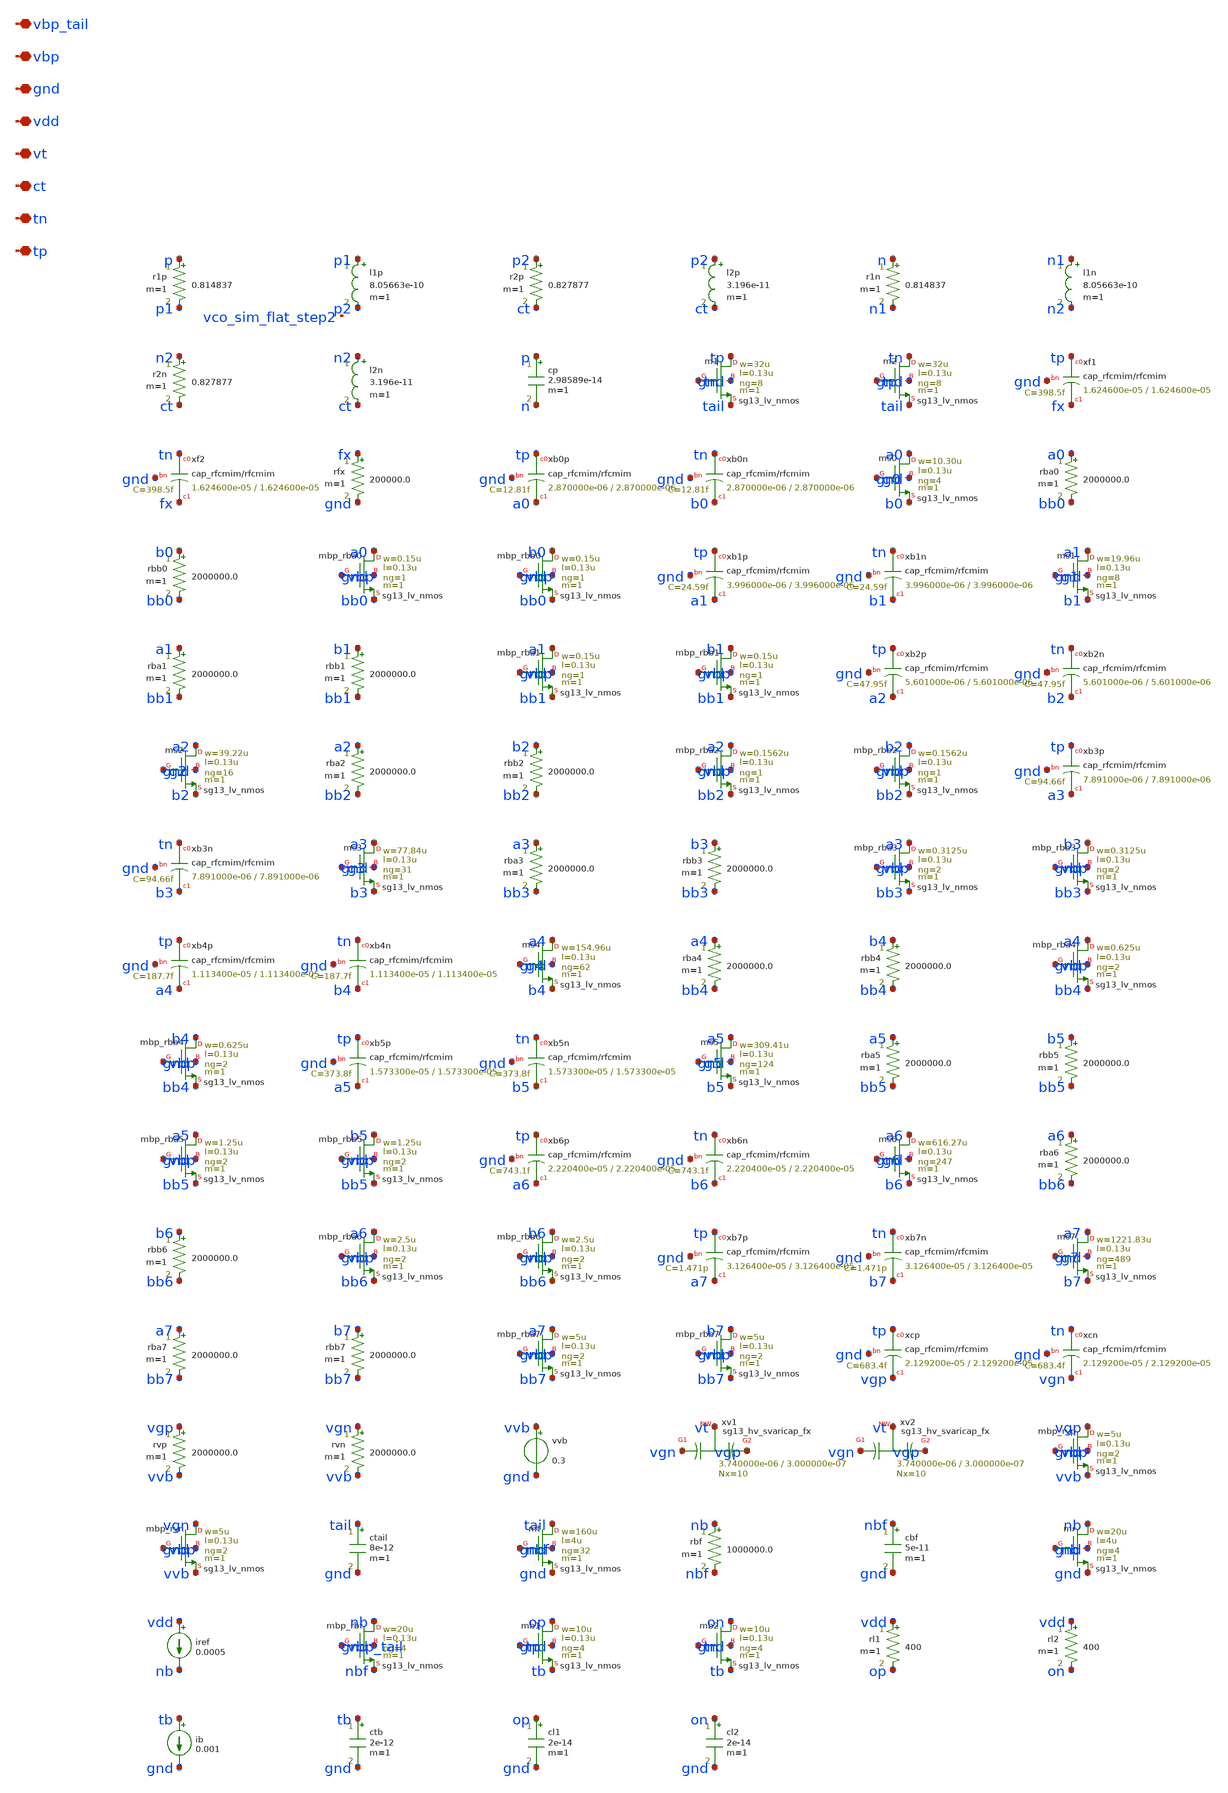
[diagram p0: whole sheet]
** sch_path: analog/vco/sch/vco_sim_flat.sch
**.subckt vco_sim_flat tp tn ct vt vdd gnd vbp vbp_tail
*.iopin tp
*.iopin tn
*.iopin ct
*.iopin vt
*.iopin vdd
*.iopin gnd
*.iopin vbp
*.iopin vbp_tail
r1p p p1 0.814837 m=1
l1p p1 p2 8.05663e-10 m=1
r2p p2 ct 0.827877 m=1
l2p p2 ct 3.196e-11 m=1
r1n n n1 0.814837 m=1
l1n n1 n2 8.05663e-10 m=1
r2n n2 ct 0.827877 m=1
l2n n2 ct 3.196e-11 m=1
cp p n 2.98589e-14 m=1
Xm1 tp tn tail gnd sg13_lv_nmos w=32u l=0.13u ng=8 m=1 mm_ok=1
Xm2 tn tp tail gnd sg13_lv_nmos w=32u l=0.13u ng=8 m=1 mm_ok=1
Xxf1 tp fx gnd cap_rfcmim w=1.624600e-05 l=1.624600e-05 wfeed=5.0e-6 m=1 mm_ok=1
Xxf2 tn fx gnd cap_rfcmim w=1.624600e-05 l=1.624600e-05 wfeed=5.0e-6 m=1 mm_ok=1
rfx fx gnd 200000.0 m=1
Xxb0p tp a0 gnd cap_rfcmim w=2.870000e-06 l=2.870000e-06 wfeed=5.0e-6 m=1 mm_ok=1
Xxb0n tn b0 gnd cap_rfcmim w=2.870000e-06 l=2.870000e-06 wfeed=5.0e-6 m=1 mm_ok=1
Xms0 a0 g0 b0 gnd sg13_lv_nmos w=10.30u l=0.13u ng=4 m=1 mm_ok=1
rba0 a0 bb0 2000000.0 m=1
rbb0 b0 bb0 2000000.0 m=1
Xmbp_rba0 a0 vbp bb0 gnd sg13_lv_nmos w=0.15u l=0.13u ng=1 m=1 mm_ok=1
Xmbp_rbb0 b0 vbp bb0 gnd sg13_lv_nmos w=0.15u l=0.13u ng=1 m=1 mm_ok=1
Xxb1p tp a1 gnd cap_rfcmim w=3.996000e-06 l=3.996000e-06 wfeed=5.0e-6 m=1 mm_ok=1
Xxb1n tn b1 gnd cap_rfcmim w=3.996000e-06 l=3.996000e-06 wfeed=5.0e-6 m=1 mm_ok=1
Xms1 a1 g1 b1 gnd sg13_lv_nmos w=19.96u l=0.13u ng=8 m=1 mm_ok=1
rba1 a1 bb1 2000000.0 m=1
rbb1 b1 bb1 2000000.0 m=1
Xmbp_rba1 a1 vbp bb1 gnd sg13_lv_nmos w=0.15u l=0.13u ng=1 m=1 mm_ok=1
Xmbp_rbb1 b1 vbp bb1 gnd sg13_lv_nmos w=0.15u l=0.13u ng=1 m=1 mm_ok=1
Xxb2p tp a2 gnd cap_rfcmim w=5.601000e-06 l=5.601000e-06 wfeed=5.0e-6 m=1 mm_ok=1
Xxb2n tn b2 gnd cap_rfcmim w=5.601000e-06 l=5.601000e-06 wfeed=5.0e-6 m=1 mm_ok=1
Xms2 a2 g2 b2 gnd sg13_lv_nmos w=39.22u l=0.13u ng=16 m=1 mm_ok=1
rba2 a2 bb2 2000000.0 m=1
rbb2 b2 bb2 2000000.0 m=1
Xmbp_rba2 a2 vbp bb2 gnd sg13_lv_nmos w=0.1562u l=0.13u ng=1 m=1 mm_ok=1
Xmbp_rbb2 b2 vbp bb2 gnd sg13_lv_nmos w=0.1562u l=0.13u ng=1 m=1 mm_ok=1
Xxb3p tp a3 gnd cap_rfcmim w=7.891000e-06 l=7.891000e-06 wfeed=5.0e-6 m=1 mm_ok=1
Xxb3n tn b3 gnd cap_rfcmim w=7.891000e-06 l=7.891000e-06 wfeed=5.0e-6 m=1 mm_ok=1
Xms3 a3 g3 b3 gnd sg13_lv_nmos w=77.84u l=0.13u ng=31 m=1 mm_ok=1
rba3 a3 bb3 2000000.0 m=1
rbb3 b3 bb3 2000000.0 m=1
Xmbp_rba3 a3 vbp bb3 gnd sg13_lv_nmos w=0.3125u l=0.13u ng=2 m=1 mm_ok=1
Xmbp_rbb3 b3 vbp bb3 gnd sg13_lv_nmos w=0.3125u l=0.13u ng=2 m=1 mm_ok=1
Xxb4p tp a4 gnd cap_rfcmim w=1.113400e-05 l=1.113400e-05 wfeed=5.0e-6 m=1 mm_ok=1
Xxb4n tn b4 gnd cap_rfcmim w=1.113400e-05 l=1.113400e-05 wfeed=5.0e-6 m=1 mm_ok=1
Xms4 a4 g4 b4 gnd sg13_lv_nmos w=154.96u l=0.13u ng=62 m=1 mm_ok=1
rba4 a4 bb4 2000000.0 m=1
rbb4 b4 bb4 2000000.0 m=1
Xmbp_rba4 a4 vbp bb4 gnd sg13_lv_nmos w=0.625u l=0.13u ng=2 m=1 mm_ok=1
Xmbp_rbb4 b4 vbp bb4 gnd sg13_lv_nmos w=0.625u l=0.13u ng=2 m=1 mm_ok=1
Xxb5p tp a5 gnd cap_rfcmim w=1.573300e-05 l=1.573300e-05 wfeed=5.0e-6 m=1 mm_ok=1
Xxb5n tn b5 gnd cap_rfcmim w=1.573300e-05 l=1.573300e-05 wfeed=5.0e-6 m=1 mm_ok=1
Xms5 a5 g5 b5 gnd sg13_lv_nmos w=309.41u l=0.13u ng=124 m=1 mm_ok=1
rba5 a5 bb5 2000000.0 m=1
rbb5 b5 bb5 2000000.0 m=1
Xmbp_rba5 a5 vbp bb5 gnd sg13_lv_nmos w=1.25u l=0.13u ng=2 m=1 mm_ok=1
Xmbp_rbb5 b5 vbp bb5 gnd sg13_lv_nmos w=1.25u l=0.13u ng=2 m=1 mm_ok=1
Xxb6p tp a6 gnd cap_rfcmim w=2.220400e-05 l=2.220400e-05 wfeed=5.0e-6 m=1 mm_ok=1
Xxb6n tn b6 gnd cap_rfcmim w=2.220400e-05 l=2.220400e-05 wfeed=5.0e-6 m=1 mm_ok=1
Xms6 a6 g6 b6 gnd sg13_lv_nmos w=616.27u l=0.13u ng=247 m=1 mm_ok=1
rba6 a6 bb6 2000000.0 m=1
rbb6 b6 bb6 2000000.0 m=1
Xmbp_rba6 a6 vbp bb6 gnd sg13_lv_nmos w=2.5u l=0.13u ng=2 m=1 mm_ok=1
Xmbp_rbb6 b6 vbp bb6 gnd sg13_lv_nmos w=2.5u l=0.13u ng=2 m=1 mm_ok=1
Xxb7p tp a7 gnd cap_rfcmim w=3.126400e-05 l=3.126400e-05 wfeed=5.0e-6 m=1 mm_ok=1
Xxb7n tn b7 gnd cap_rfcmim w=3.126400e-05 l=3.126400e-05 wfeed=5.0e-6 m=1 mm_ok=1
Xms7 a7 g7 b7 gnd sg13_lv_nmos w=1221.83u l=0.13u ng=489 m=1 mm_ok=1
rba7 a7 bb7 2000000.0 m=1
rbb7 b7 bb7 2000000.0 m=1
Xmbp_rba7 a7 vbp bb7 gnd sg13_lv_nmos w=5u l=0.13u ng=2 m=1 mm_ok=1
Xmbp_rbb7 b7 vbp bb7 gnd sg13_lv_nmos w=5u l=0.13u ng=2 m=1 mm_ok=1
Xxcp tp vgp gnd cap_rfcmim w=2.129200e-05 l=2.129200e-05 wfeed=5.0e-6 m=1 mm_ok=1
Xxcn tn vgn gnd cap_rfcmim w=2.129200e-05 l=2.129200e-05 wfeed=5.0e-6 m=1 mm_ok=1
rvp vgp vvb 2000000.0 m=1
rvn vgn vvb 2000000.0 m=1
vvb vvb gnd 0.3
Xxv1 vgn vt vgp sub! sg13_hv_svaricap_fx w=3.740000e-06 l=3.000000e-07 Nx=10 mm_ok=1
Xxv2 vgn vt vgp sub! sg13_hv_svaricap_fx w=3.740000e-06 l=3.000000e-07 Nx=10 mm_ok=1
Xmbp_rvp vgp vbp vvb gnd sg13_lv_nmos w=5u l=0.13u ng=2 m=1 mm_ok=1
Xmbp_rvn vgn vbp vvb gnd sg13_lv_nmos w=5u l=0.13u ng=2 m=1 mm_ok=1
ctail tail gnd 8e-12 m=1
Xmt tail nbf gnd gnd sg13_lv_nmos w=160u l=4u ng=32 m=1 mm_ok=1
rbf nb nbf 1000000.0 m=1
cbf nbf gnd 5e-11 m=1
Xmr nb nb gnd gnd sg13_lv_nmos w=20u l=4u ng=4 m=1 mm_ok=1
iref vdd nb 0.0005
Xmbp_rbf nb vbp_tail nbf gnd sg13_lv_nmos w=20u l=0.13u ng=4 m=1 mm_ok=1
Xmb1 op tp tb gnd sg13_lv_nmos w=10u l=0.13u ng=4 m=1 mm_ok=1
Xmb2 on tn tb gnd sg13_lv_nmos w=10u l=0.13u ng=4 m=1 mm_ok=1
rl1 vdd op 400 m=1
rl2 vdd on 400 m=1
ib tb gnd 0.001
ctb tb gnd 2e-12 m=1
cl1 op gnd 2e-14 m=1
cl2 on gnd 2e-14 m=1
**.ends
.end
